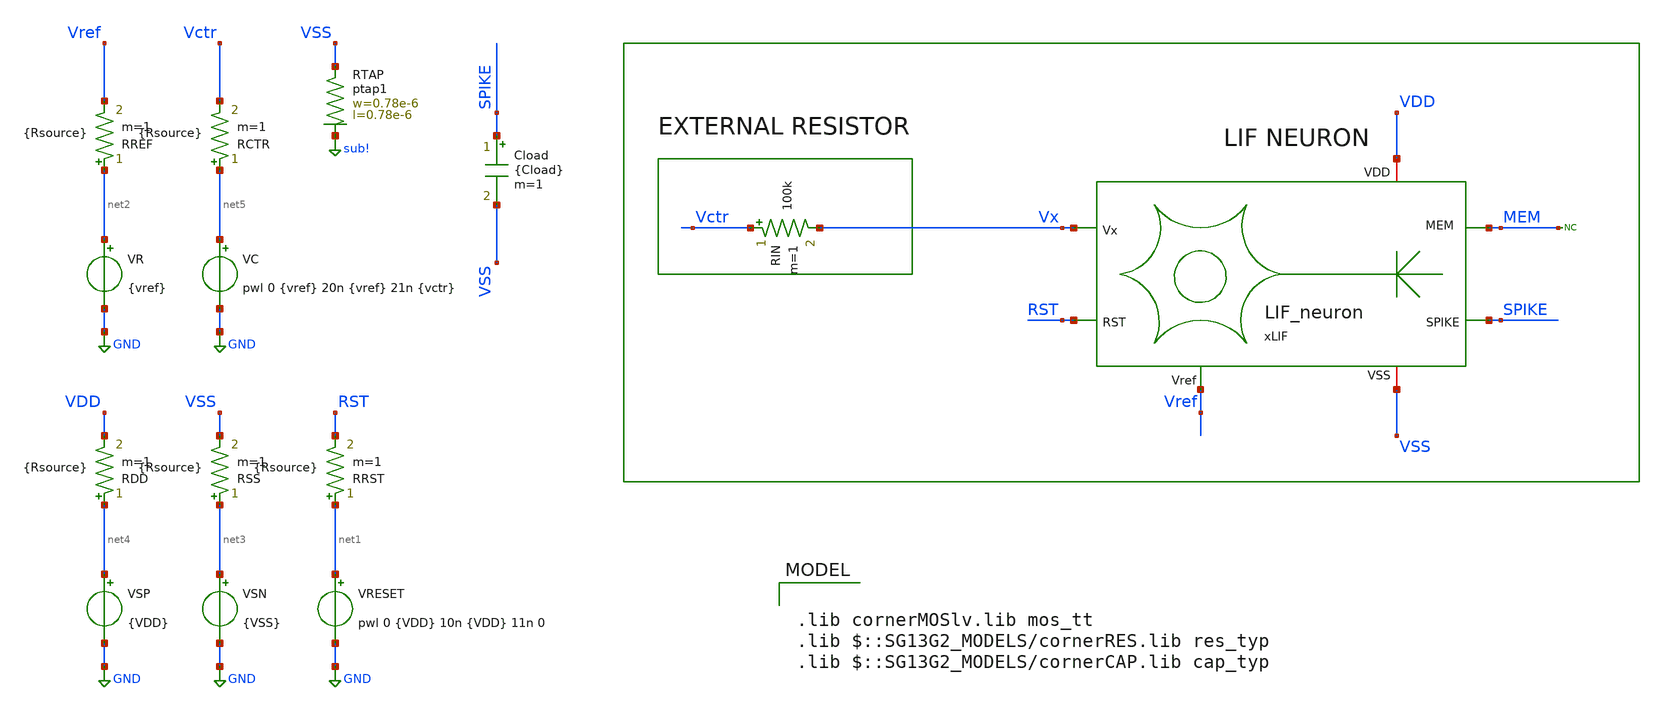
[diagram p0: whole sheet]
** sch_path: work/LIF_neuron/xschem/LIF_neuron_tb.sch
**.subckt LIF_neuron_tb
VRESET net1 GND pwl 0 {VDD} 10n {VDD} 11n 0
VSN net3 GND {VSS}
VR net2 GND {vref}
VC net5 GND pwl 0 {vref} 20n {vref} 21n {vctr}
xLIF VDD Vx MEM RST SPIKE VSS Vref LIF_neuron
RDD net4 VDD {Rsource} m=1
RSS net3 VSS {Rsource} m=1
RRST net1 RST {Rsource} m=1
RREF net2 Vref {Rsource} m=1
RCTR net5 Vctr {Rsource} m=1
Cload SPIKE VSS {Cload} m=1
RIN Vctr Vx 100k m=1
VSP net4 GND {VDD}
* noconn MEM
XRTAP VSS sub! ptap1 R=262.8 w=0.78e-6 l=0.78e-6
**** begin user architecture code



.param VDD = 1.17
.param VSS = 0
.param vctr = 0.6
.param vref = 1.2
.param Cload = 0.1p
.param Rsource = 1m

.param sw_stat_global = 0
.param sw_stat_mismatch = 0

.save all

.control

* >> Variables <<

let Vhigh = 1.17
let Vmid = Vhigh * 0.5

let tstop = 0.1u
let tstep = tstop/2.5k

* Run transient analysis
tran $&tstep $&tstop

let IDD = -1*i(VSP)
meas tran I_avg AVG IDD from=tstep to=tstop
let P_avg = abs(I_avg*Vhigh)

meas TRAN T_spk TRIG v(SPIKE) VAL=Vmid rise=2 TARG v(SPIKE) VAL=Vmid rise=3
let F_spk = 1 / T_spk

let E_spk = P_avg/F_spk

*Print results
print F_spk I_avg P_avg E_spk

* Plots
plot v(Vctr) v(Vref) v(RST)
plot v(MEM) v(Vx)
plot v(xLIF.COMP)
plot v(SPIKE)

.endc



.lib cornerMOSlv.lib mos_tt
.lib $::SG13G2_MODELS/cornerRES.lib res_typ
.lib $::SG13G2_MODELS/cornerCAP.lib cap_typ

**** end user architecture code
**.ends
.GLOBAL GND
.GLOBAL sub!
.end
